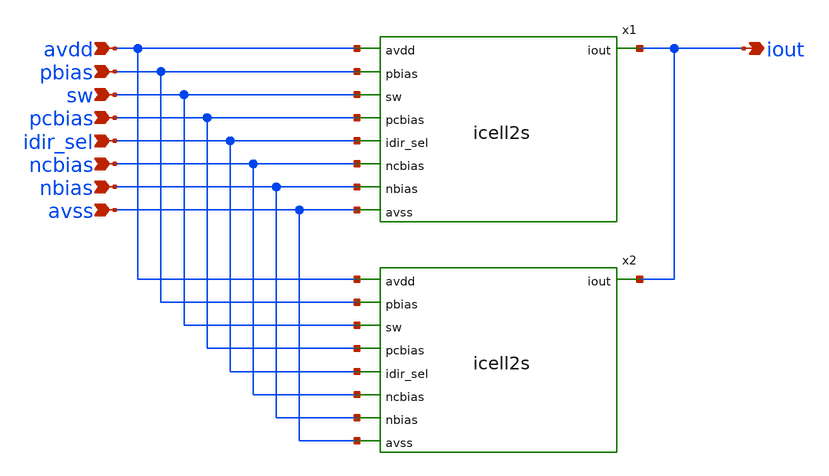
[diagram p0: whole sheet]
** sch_path: xschem/icell4s.sch
**.subckt icell4s avdd pbias sw pcbias idir_sel ncbias nbias avss iout
*.ipin avdd
*.ipin pbias
*.ipin sw
*.ipin pcbias
*.ipin idir_sel
*.ipin ncbias
*.ipin nbias
*.ipin avss
*.opin iout
x1 avdd iout pbias sw pcbias idir_sel ncbias nbias avss icell2s
x2 avdd iout pbias sw pcbias idir_sel ncbias nbias avss icell2s
**.ends
.end
